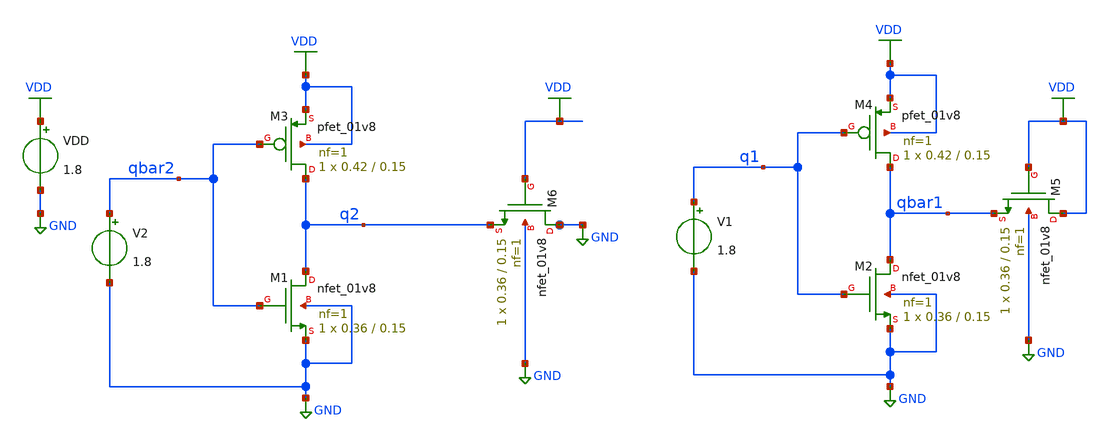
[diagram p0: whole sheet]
** sch_path: nikhil/SRAM/6T_SRAM_write_SNM.sch
**.subckt 6T_SRAM_write_SNM
XM2 qbar1 q1 GND GND sky130_fd_pr__nfet_01v8 L=0.15 W=0.36 nf=1 ad='int((nf+1)/2) * W/nf * 0.29' as='int((nf+2)/2) * W/nf * 0.29'
+ pd='2*int((nf+1)/2) * (W/nf + 0.29)' ps='2*int((nf+2)/2) * (W/nf + 0.29)' nrd='0.29 / W' nrs='0.29 / W'
+ sa=0 sb=0 sd=0 mult=1 m=1
XM4 qbar1 q1 VDD VDD sky130_fd_pr__pfet_01v8 L=0.15 W=0.42 nf=1 ad='int((nf+1)/2) * W/nf * 0.29' as='int((nf+2)/2) * W/nf * 0.29'
+ pd='2*int((nf+1)/2) * (W/nf + 0.29)' ps='2*int((nf+2)/2) * (W/nf + 0.29)' nrd='0.29 / W' nrs='0.29 / W'
+ sa=0 sb=0 sd=0 mult=1 m=1
VDD VDD GND 1.8
V1 q1 GND 1.8
XM1 q2 qbar2 GND GND sky130_fd_pr__nfet_01v8 L=0.15 W=0.36 nf=1 ad='int((nf+1)/2) * W/nf * 0.29' as='int((nf+2)/2) * W/nf * 0.29'
+ pd='2*int((nf+1)/2) * (W/nf + 0.29)' ps='2*int((nf+2)/2) * (W/nf + 0.29)' nrd='0.29 / W' nrs='0.29 / W'
+ sa=0 sb=0 sd=0 mult=1 m=1
XM3 q2 qbar2 VDD VDD sky130_fd_pr__pfet_01v8 L=0.15 W=0.42 nf=1 ad='int((nf+1)/2) * W/nf * 0.29' as='int((nf+2)/2) * W/nf * 0.29'
+ pd='2*int((nf+1)/2) * (W/nf + 0.29)' ps='2*int((nf+2)/2) * (W/nf + 0.29)' nrd='0.29 / W' nrs='0.29 / W'
+ sa=0 sb=0 sd=0 mult=1 m=1
V2 qbar2 GND 1.8
XM5 VDD VDD qbar1 GND sky130_fd_pr__nfet_01v8 L=0.15 W=0.36 nf=1 ad='int((nf+1)/2) * W/nf * 0.29' as='int((nf+2)/2) * W/nf * 0.29'
+ pd='2*int((nf+1)/2) * (W/nf + 0.29)' ps='2*int((nf+2)/2) * (W/nf + 0.29)' nrd='0.29 / W' nrs='0.29 / W'
+ sa=0 sb=0 sd=0 mult=1 m=1
XM6 GND VDD q2 GND sky130_fd_pr__nfet_01v8 L=0.15 W=0.36 nf=1 ad='int((nf+1)/2) * W/nf * 0.29' as='int((nf+2)/2) * W/nf * 0.29'
+ pd='2*int((nf+1)/2) * (W/nf + 0.29)' ps='2*int((nf+2)/2) * (W/nf + 0.29)' nrd='0.29 / W' nrs='0.29 / W'
+ sa=0 sb=0 sd=0 mult=1 m=1
**** begin user architecture code

.dc


.options wnflag=1
.include /pdk/open_pdks/sources/sky130-pdk/libraries/sky130_fd_pr/latest/cells/nfet_01v8/sky130_fd_pr__nfet_01v8__tt.corner.spice
.include /pdk/open_pdks/sources/sky130-pdk/libraries/sky130_fd_pr/latest/cells/nfet_01v8_lvt/sky130_fd_pr__nfet_01v8_lvt__tt.corner.spice
.include /pdk/open_pdks/sources/sky130-pdk/libraries/sky130_fd_pr/latest/cells/pfet_01v8/sky130_fd_pr__pfet_01v8__tt.corner.spice
.include /pdk/open_pdks/sources/sky130-pdk/libraries/sky130_fd_pr/latest/cells/nfet_03v3_nvt/sky130_fd_pr__nfet_03v3_nvt__tt.corner.spice
.include /pdk/open_pdks/sources/sky130-pdk/libraries/sky130_fd_pr/latest/cells/nfet_05v0_nvt/sky130_fd_pr__nfet_05v0_nvt__tt.corner.spice
.include /pdk/open_pdks/sources/sky130-pdk/libraries/sky130_fd_pr/latest/cells/esd_nfet_01v8/sky130_fd_pr__esd_nfet_01v8__tt.corner.spice
.include /pdk/open_pdks/sources/sky130-pdk/libraries/sky130_fd_pr/latest/cells/pfet_01v8_lvt/sky130_fd_pr__pfet_01v8_lvt__tt.corner.spice
.include /pdk/open_pdks/sources/sky130-pdk/libraries/sky130_fd_pr/latest/cells/pfet_01v8_hvt/sky130_fd_pr__pfet_01v8_hvt__tt.corner.spice
.include /pdk/open_pdks/sources/sky130-pdk/libraries/sky130_fd_pr/latest/cells/esd_pfet_g5v0d10v5/sky130_fd_pr__esd_pfet_g5v0d10v5__tt.corner.spice
.include /pdk/open_pdks/sources/sky130-pdk/libraries/sky130_fd_pr/latest/cells/pfet_g5v0d10v5/sky130_fd_pr__pfet_g5v0d10v5__tt.corner.spice
.include /pdk/open_pdks/sources/sky130-pdk/libraries/sky130_fd_pr/latest/cells/pfet_g5v0d16v0/sky130_fd_pr__pfet_g5v0d16v0__tt.corner.spice
.include /pdk/open_pdks/sources/sky130-pdk/libraries/sky130_fd_pr/latest/cells/nfet_g5v0d10v5/sky130_fd_pr__nfet_g5v0d10v5__tt.corner.spice
.include /pdk/open_pdks/sources/sky130-pdk/libraries/sky130_fd_pr/latest/cells/nfet_g5v0d16v0/sky130_fd_pr__nfet_g5v0d16v0__tt_discrete.corner.spice
.include /pdk/open_pdks/sources/sky130-pdk/libraries/sky130_fd_pr/latest/cells/esd_nfet_g5v0d10v5/sky130_fd_pr__esd_nfet_g5v0d10v5__tt.corner.spice
.include /pdk/open_pdks/sources/sky130-pdk/libraries/sky130_fd_pr/latest/models/corners/tt/nonfet.spice
* Mismatch parameters
.include /pdk/open_pdks/sources/sky130-pdk/libraries/sky130_fd_pr/latest/cells/nfet_01v8/sky130_fd_pr__nfet_01v8__mismatch.corner.spice
.include /pdk/open_pdks/sources/sky130-pdk/libraries/sky130_fd_pr/latest/cells/pfet_01v8/sky130_fd_pr__pfet_01v8__mismatch.corner.spice
.include /pdk/open_pdks/sources/sky130-pdk/libraries/sky130_fd_pr/latest/cells/nfet_01v8_lvt/sky130_fd_pr__nfet_01v8_lvt__mismatch.corner.spice
.include /pdk/open_pdks/sources/sky130-pdk/libraries/sky130_fd_pr/latest/cells/pfet_01v8_lvt/sky130_fd_pr__pfet_01v8_lvt__mismatch.corner.spice
.include /pdk/open_pdks/sources/sky130-pdk/libraries/sky130_fd_pr/latest/cells/pfet_01v8_hvt/sky130_fd_pr__pfet_01v8_hvt__mismatch.corner.spice
.include /pdk/open_pdks/sources/sky130-pdk/libraries/sky130_fd_pr/latest/cells/nfet_g5v0d10v5/sky130_fd_pr__nfet_g5v0d10v5__mismatch.corner.spice
.include /pdk/open_pdks/sources/sky130-pdk/libraries/sky130_fd_pr/latest/cells/pfet_g5v0d10v5/sky130_fd_pr__pfet_g5v0d10v5__mismatch.corner.spice
.include /pdk/open_pdks/sources/sky130-pdk/libraries/sky130_fd_pr/latest/cells/nfet_05v0_nvt/sky130_fd_pr__nfet_05v0_nvt__mismatch.corner.spice
.include /pdk/open_pdks/sources/sky130-pdk/libraries/sky130_fd_pr/latest/cells/nfet_03v3_nvt/sky130_fd_pr__nfet_03v3_nvt__mismatch.corner.spice
* Resistor$::SKYWATER_MODELS/Capacitor
.include /pdk/open_pdks/sources/sky130-pdk/libraries/sky130_fd_pr/latest/models/r+c/res_typical__cap_typical.spice
.include /pdk/open_pdks/sources/sky130-pdk/libraries/sky130_fd_pr/latest/models/r+c/res_typical__cap_typical__lin.spice
* Special cells
.include /pdk/open_pdks/sources/sky130-pdk/libraries/sky130_fd_pr/latest/models/corners/tt/specialized_cells.spice
* All models
.include /pdk/open_pdks/sources/sky130-pdk/libraries/sky130_fd_pr/latest/models/all.spice
* Corner
.include /pdk/open_pdks/sources/sky130-pdk/libraries/sky130_fd_pr/latest/models/corners/tt/rf.spice

**** end user architecture code
**.ends
.GLOBAL GND
.GLOBAL VDD
.end
